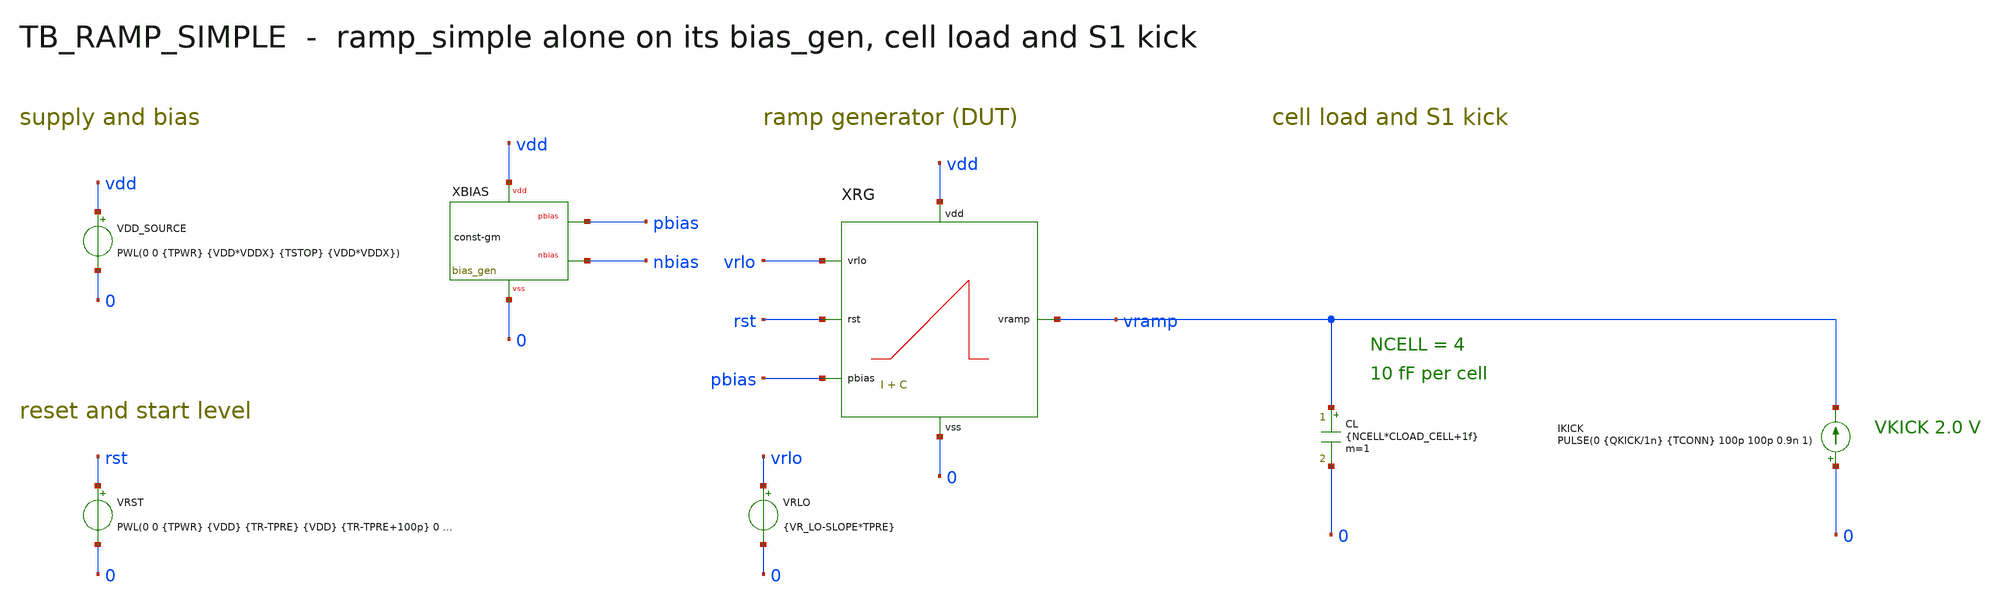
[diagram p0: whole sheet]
** sch_path: mixed_signal/ramp_gen/tb_ramp_simple.sch
**.subckt tb_ramp_simple
VDD_SOURCE vdd 0 PWL(0 0 {TPWR} {VDD*VDDX} {TSTOP} {VDD*VDDX})
XBIAS vdd 0 pbias nbias bias_gen
VRST rst 0 PWL(0 0 {TPWR} {VDD} {TR-TPRE} {VDD} {TR-TPRE+100p} 0 {TRST2} 0 {TRST2+100p} {VDD})
VRLO vrlo 0 {VR_LO-SLOPE*TPRE}
XRG vramp rst vrlo pbias vdd 0 ramp_simple
CL vramp 0 {NCELL*CLOAD_CELL+1f} m=1
IKICK 0 vramp PULSE(0 {QKICK/1n} {TCONN} 100p 100p 0.9n 1)
**** begin user architecture code

.include /foss/pdks/gf180mcuD/libs.tech/ngspice/design.ngspice
.lib /foss/pdks/gf180mcuD/libs.tech/ngspice/sm141064.ngspice typical
.lib /foss/pdks/gf180mcuD/libs.tech/ngspice/sm141064.ngspice res_typical
.lib /foss/pdks/gf180mcuD/libs.tech/ngspice/sm141064.ngspice mimcap_typical
.lib /foss/pdks/gf180mcuD/libs.tech/ngspice/sm141064.ngspice moscap_typical
.include /foss/designs/mixed_signal/ramp_gen/ref/bias_gen/data/bias_gen_params.spice
.include /foss/designs/mixed_signal/ramp_gen/ref/bias_gen/bias_gen.spice
.include /foss/designs/mixed_signal/ramp_gen/data/ramp_simple_params.spice


.param VDD=3.3
.param TCOUNT=50n
.param VR_LO=0.5
.param VR_HI=2.0
.param LSB='(VR_HI-VR_LO)/256'
.param TRAMP='256*TCOUNT'
.param SLOPE='(VR_HI-VR_LO)/TRAMP'
.param CLOAD_CELL=10f
.param NCELL=4
.param VKICK=2.0
.param VDDX=1
.param TPRE=0
.param TPWR=100n
.param T0=1u
.param TS='T0+300n'
.param TCONN='TS+10n'
.param TR='T0+400n'
.param TE='TR+TRAMP'
.param TOVR='20*TCOUNT'
.param TRST2='TE+TOVR+50n'
.param TSTOP='TRST2+600n'
.param QKICK='NCELL*CLOAD_CELL*(VKICK-VR_LO)'


.options reltol=1e-5 abstol=1e-13 vntol=1e-7 gmin=1e-15 savecurrents
.tran 0.2n {TSTOP} 0 2n
.save v(vramp) v(vrlo) v(rst) v(pbias) i(vdd_source)
.save @m.xrg.xps.m0[vds] @m.xrg.xps.m0[vdsat] @m.xrg.xps.m0[id]
.measure tran vr_tconn FIND v(vramp) AT={TCONN}
.measure tran vr_kick_max MAX v(vramp) FROM={TCONN} TO={TR}
.measure tran vr_tr FIND v(vramp) AT={TR}
.measure tran vr_te FIND v(vramp) AT={TE}
.measure tran vr_ovr FIND v(vramp) AT={TE+TOVR}
.measure tran i_ps AVG @m.xrg.xps.m0[id] FROM={TR} TO={TE}
.measure tran i_total AVG i(vdd_source) FROM={TR} TO={TE}
.measure tran ps_vds_top FIND @m.xrg.xps.m0[vds] AT={TE+TOVR}
.measure tran ps_vdsat FIND @m.xrg.xps.m0[vdsat] AT={TE+TOVR}
.measure tran ps_margin PARAM='abs(ps_vds_top)-abs(ps_vdsat)'
.measure tran pbias_tr FIND v(pbias) AT={TR}
.control
set num_threads=1
set wr_singlescale
set wr_vecnames
run
wrdata ramp.csv v(vramp) v(vrlo) v(rst) v(pbias)
quit
.endc

**** end user architecture code
**.ends
.end
